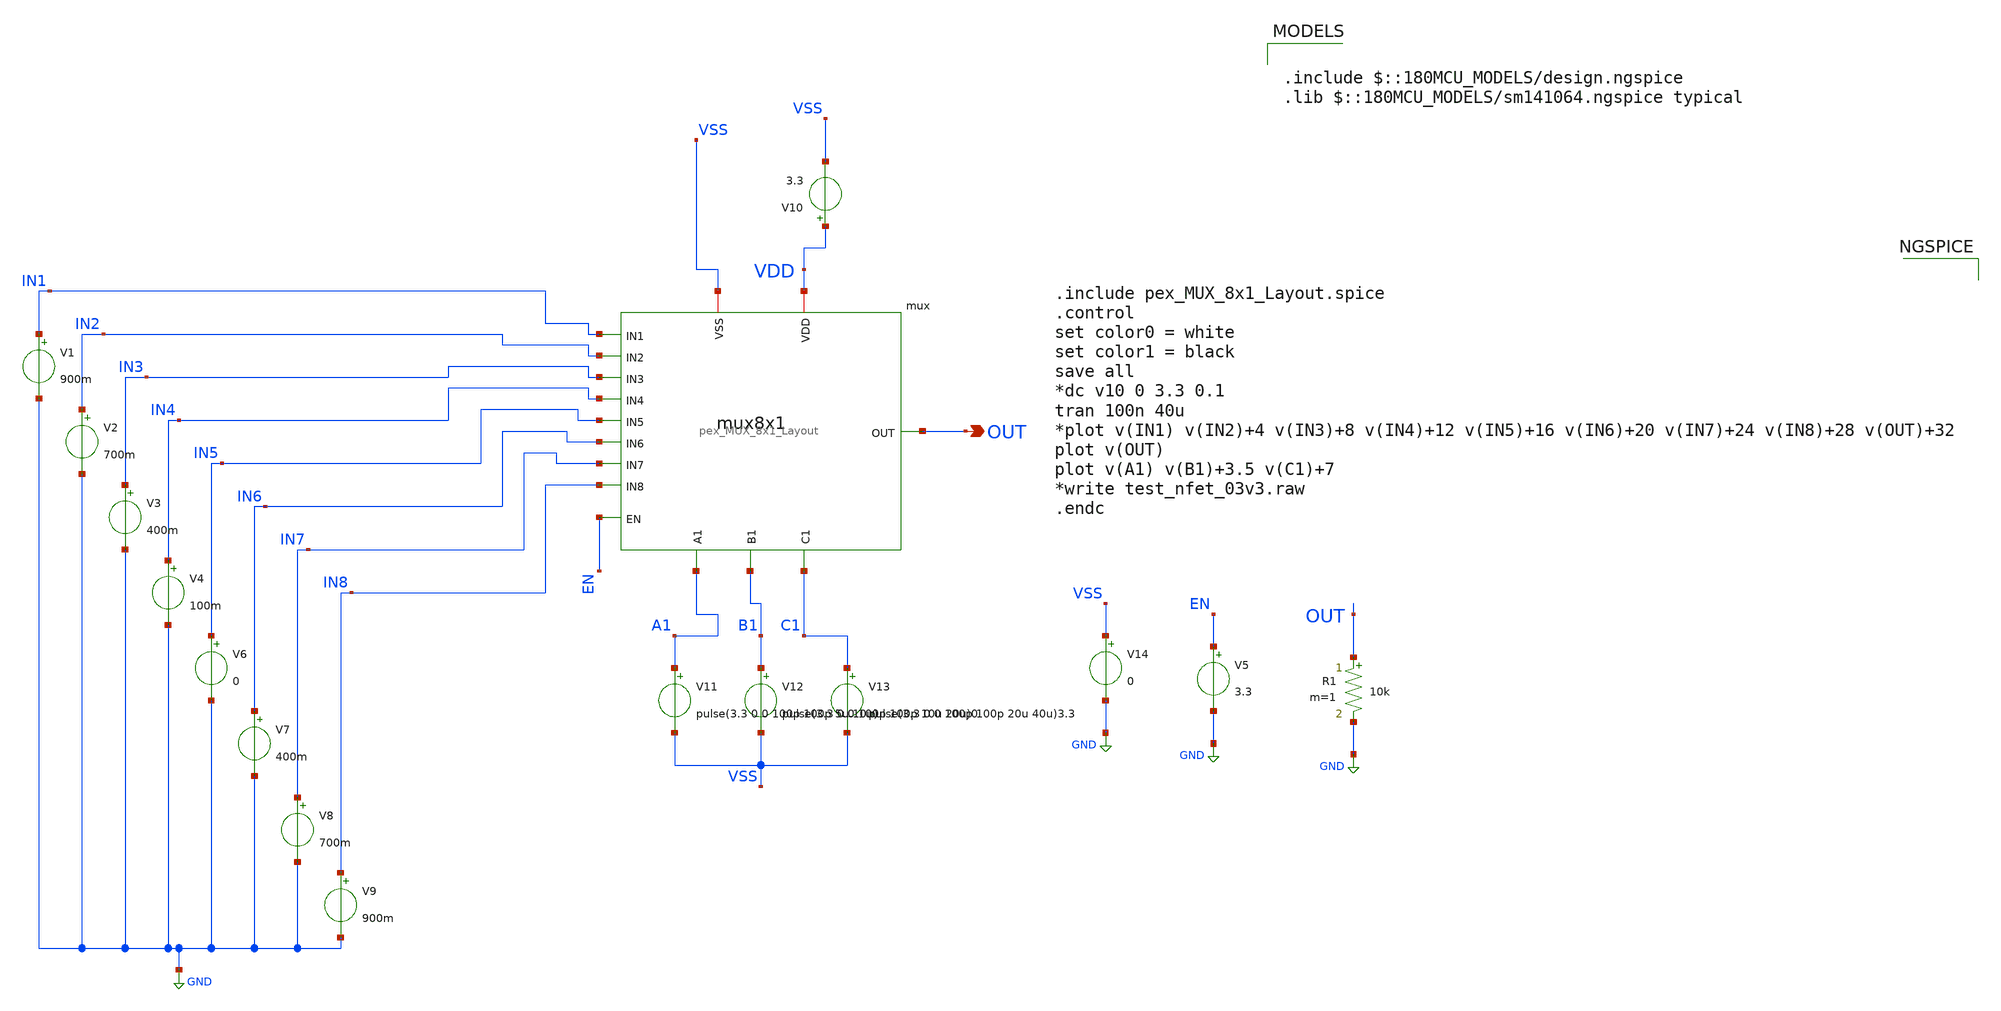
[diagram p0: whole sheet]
** sch_path: SCOP_INPUT_AND_MUX_PAKISTAN_03/Xschem/MUX_8x1/muxWnonovpclkTB.sch
**.subckt muxWnonovpclkTB OUT
*.opin OUT
V1 IN1 GND 900m
V2 IN2 GND 700m
V3 IN3 GND 400m
V4 IN4 GND 100m
V6 IN5 GND 0
V7 IN6 GND 400m
V8 IN7 GND 700m
V9 IN8 GND 900m
V10 VDD VSS 3.3
V11 A1 VSS pulse(3.3 0 0 100p 100p 5u 10u)
V12 B1 VSS pulse(3.3 0 0 100p 100p 10u 20u)0
V13 C1 VSS pulse(3.3 0 0 100p 100p 20u 40u)3.3
V14 VSS GND 0
V5 EN GND 3.3
R1 OUT GND 10k m=1
x1 VSS VDD IN1 IN2 IN3 B1 IN4 OUT IN5 C1 IN6 IN7 IN8 A1 EN pex_MUX_8x1_Layout
**** begin user architecture code

.include $::180MCU_MODELS/design.ngspice
.lib $::180MCU_MODELS/sm141064.ngspice typical



.include pex_MUX_8x1_Layout.spice
.control
set color0 = white
set color1 = black
save all
*dc v10 0 3.3 0.1
tran 100n 40u
*plot v(IN1) v(IN2)+4 v(IN3)+8 v(IN4)+12 v(IN5)+16 v(IN6)+20 v(IN7)+24 v(IN8)+28 v(OUT)+32
plot v(OUT)
plot v(A1) v(B1)+3.5 v(C1)+7
*write test_nfet_03v3.raw
.endc


**** end user architecture code
**.ends
.GLOBAL GND
.end
